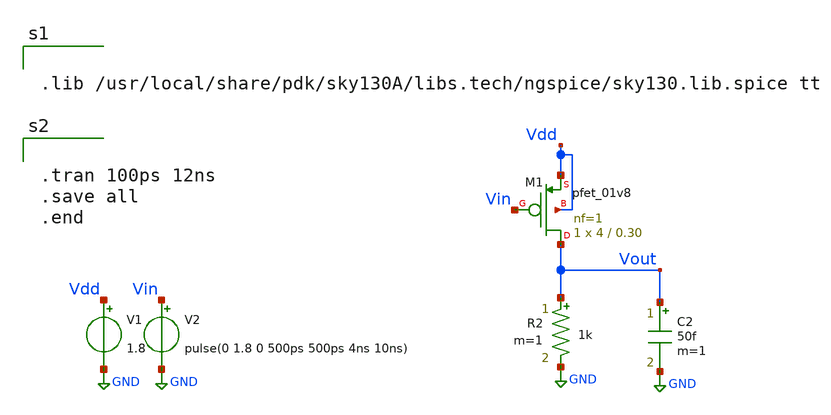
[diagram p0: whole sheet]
** sch_path: xschem files/pmos_as_inverter.sch
**.subckt pmos_as_inverter
V1 Vdd GND 1.8
V2 Vin GND pulse(0 1.8 0 500ps 500ps 4ns 10ns)
XM1 Vout Vin Vdd Vdd sky130_fd_pr__pfet_01v8 L=0.30 W=4 nf=1 ad='int((nf+1)/2) * W/nf * 0.29' as='int((nf+2)/2) * W/nf * 0.29'
+ pd='2*int((nf+1)/2) * (W/nf + 0.29)' ps='2*int((nf+2)/2) * (W/nf + 0.29)' nrd='0.29 / W' nrs='0.29 / W'
+ sa=0 sb=0 sd=0 mult=1 m=1
R2 Vout GND 1k m=1
C2 Vout GND 50f m=1
**** begin user architecture code


.lib /usr/local/share/pdk/sky130A/libs.tech/ngspice/sky130.lib.spice tt




.tran 100ps 12ns
.save all
.end


**** end user architecture code
**.ends
.GLOBAL GND
.end
